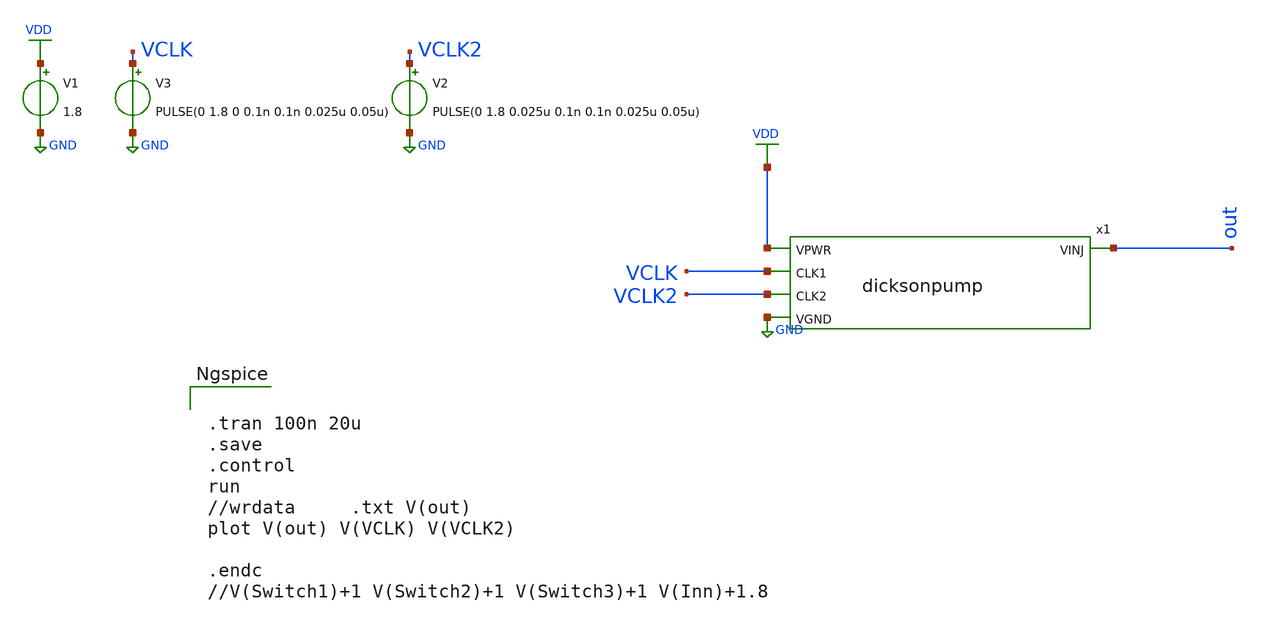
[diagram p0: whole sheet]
** sch_path: sky130_cells/ChargePump/DicksonPump_TB.sch
**.subckt DicksonPump_TB
V3 VCLK GND PULSE(0 1.8 0 0.1n 0.1n 0.025u 0.05u)
V1 VDD GND 1.8
V2 VCLK2 GND PULSE(0 1.8 0.025u 0.1n 0.1n 0.025u 0.05u)
x1 VDD out VCLK VCLK2 GND dicksonpump
**** begin user architecture code

** opencircuitdesign pdks install
.lib $::SKYWATER_MODELS/sky130.lib.spice tt




.tran 100n 20u
.save
.control
run
//wrdata     .txt V(out)
plot V(out) V(VCLK) V(VCLK2)

.endc
//V(Switch1)+1 V(Switch2)+1 V(Switch3)+1 V(Inn)+1.8


**** end user architecture code
**.ends

* expanding   symbol:  sky130_cells/ChargePump/dicksonpump.sym # of pins=5
** sym_path: sky130_cells/ChargePump/dicksonpump.sym
** sch_path: sky130_cells/ChargePump/dicksonpump.sch
.subckt dicksonpump VPWR VINJ CLK1 CLK2 VGND
*.opin VINJ
*.ipin VPWR
*.ipin CLK1
*.ipin CLK2
*.ipin VGND
D1 VPWR net1 sky130_fd_pr__diode_pw2nd_11v0 area=50
D2 net1 net2 sky130_fd_pr__diode_pw2nd_11v0 area=50
D3 net2 net3 sky130_fd_pr__diode_pw2nd_11v0 area=50
D4 net3 net4 sky130_fd_pr__diode_pw2nd_11v0 area=50
D5 net4 VINJ sky130_fd_pr__diode_pw2nd_11v0 area=50
XC1 net1 CLK1 sky130_fd_pr__cap_mim_m3_1 W=15 L=5 MF=1 m=1
XC2 CLK1 net1 sky130_fd_pr__cap_mim_m3_2 W=15 L=5 MF=1 m=1
XC3 net2 CLK2 sky130_fd_pr__cap_mim_m3_1 W=15 L=5 MF=1 m=1
XC4 CLK2 net2 sky130_fd_pr__cap_mim_m3_2 W=15 L=5 MF=1 m=1
XC5 net3 CLK1 sky130_fd_pr__cap_mim_m3_1 W=15 L=5 MF=1 m=1
XC6 CLK1 net3 sky130_fd_pr__cap_mim_m3_2 W=15 L=5 MF=1 m=1
XC7 net4 CLK2 sky130_fd_pr__cap_mim_m3_1 W=15 L=5 MF=1 m=1
XC8 CLK2 net4 sky130_fd_pr__cap_mim_m3_2 W=15 L=5 MF=1 m=1
XC9 VINJ net5 sky130_fd_pr__cap_mim_m3_1 W=80 L=5 MF=1 m=1
XC10 VGND VINJ sky130_fd_pr__cap_mim_m3_2 W=80 L=5 MF=1 m=1
.ends

.GLOBAL GND
.GLOBAL VDD
.end
